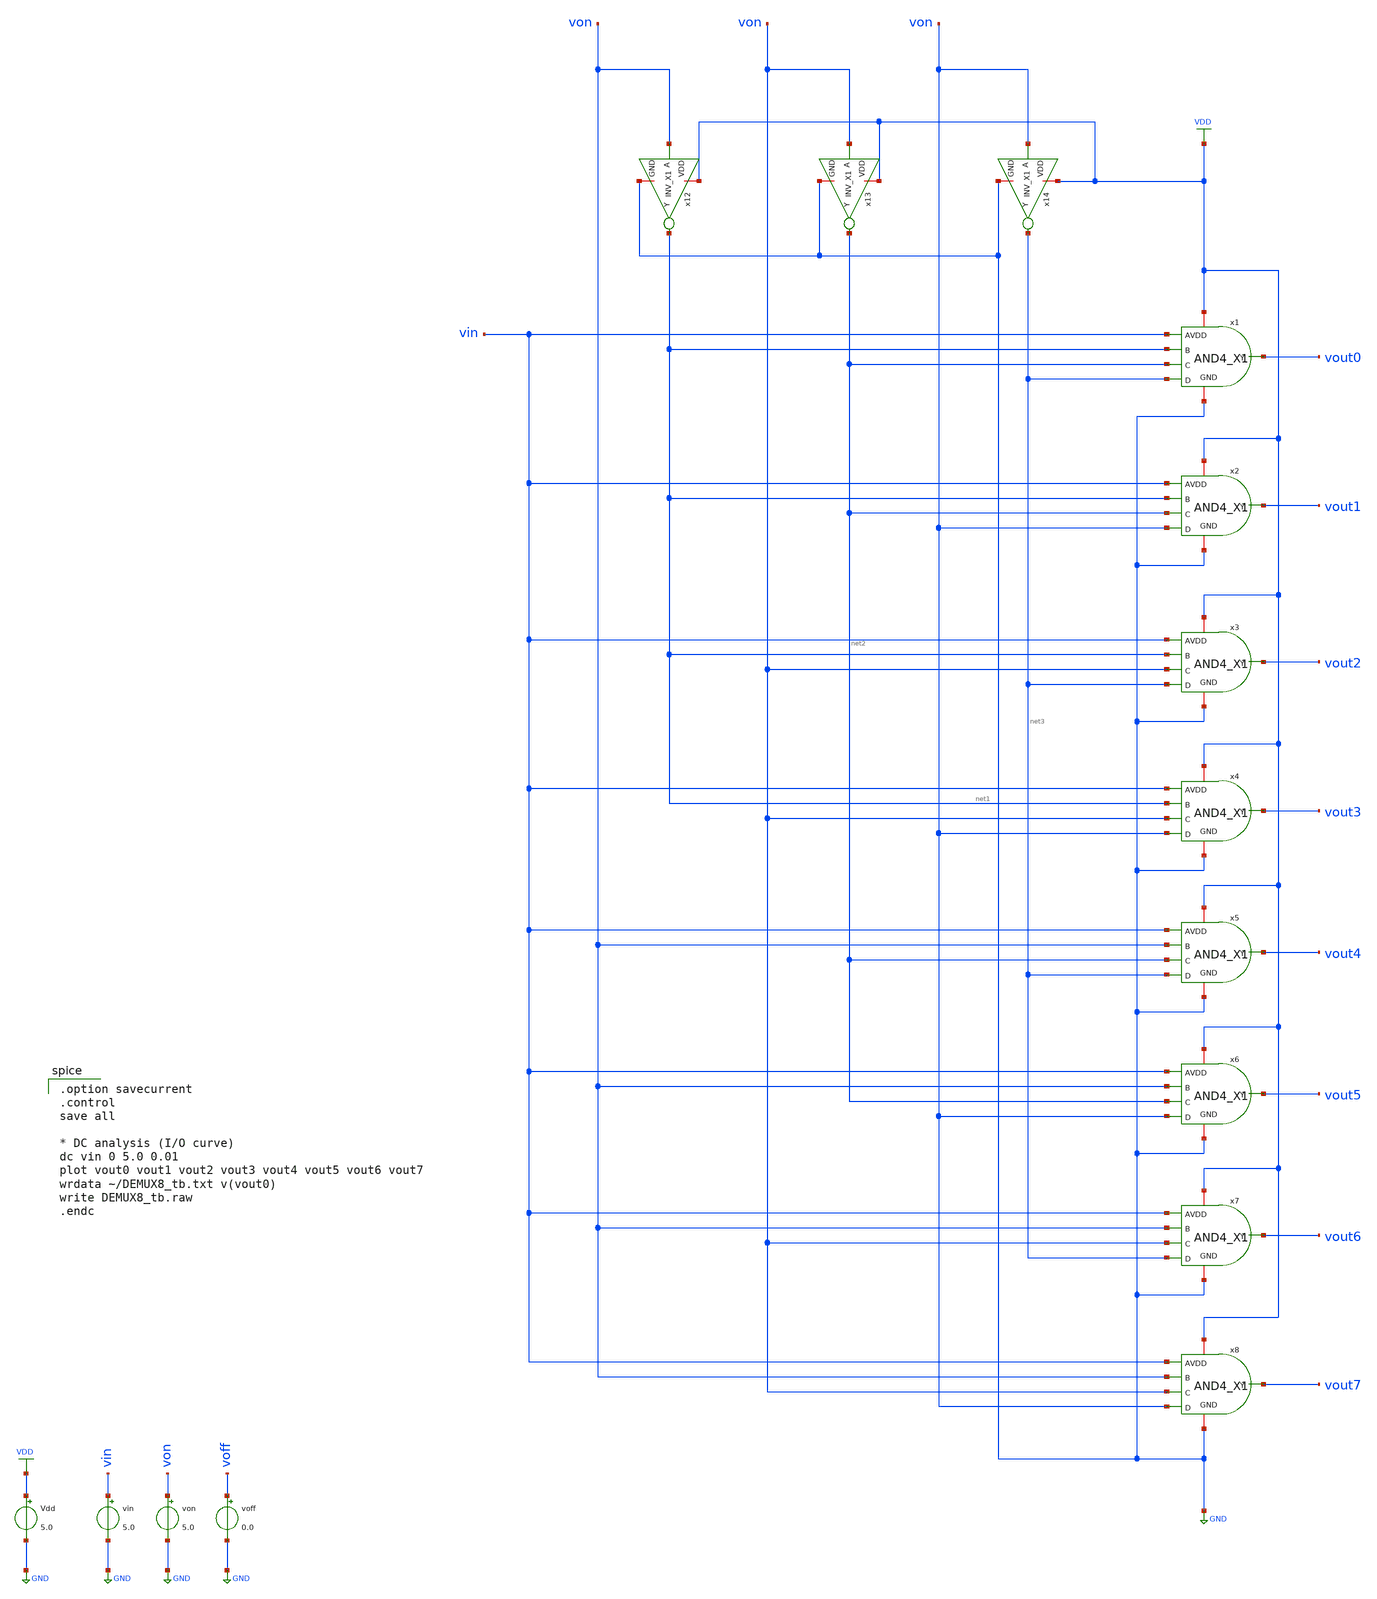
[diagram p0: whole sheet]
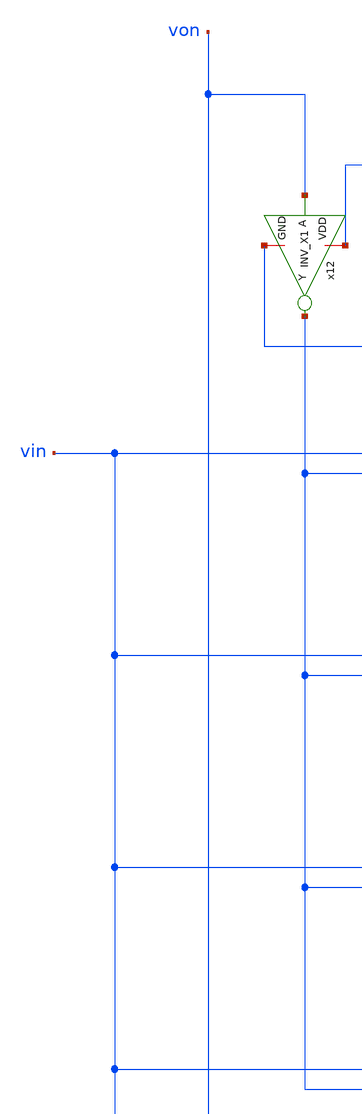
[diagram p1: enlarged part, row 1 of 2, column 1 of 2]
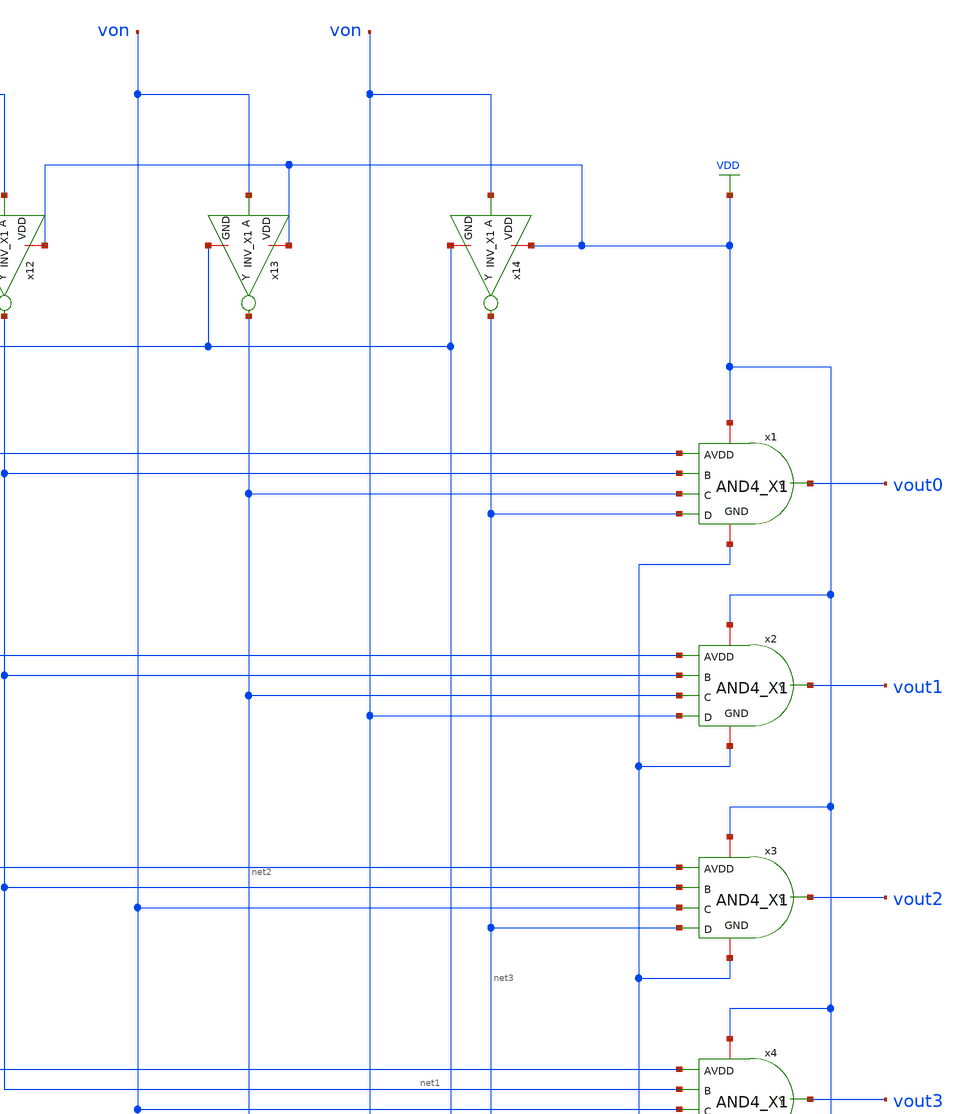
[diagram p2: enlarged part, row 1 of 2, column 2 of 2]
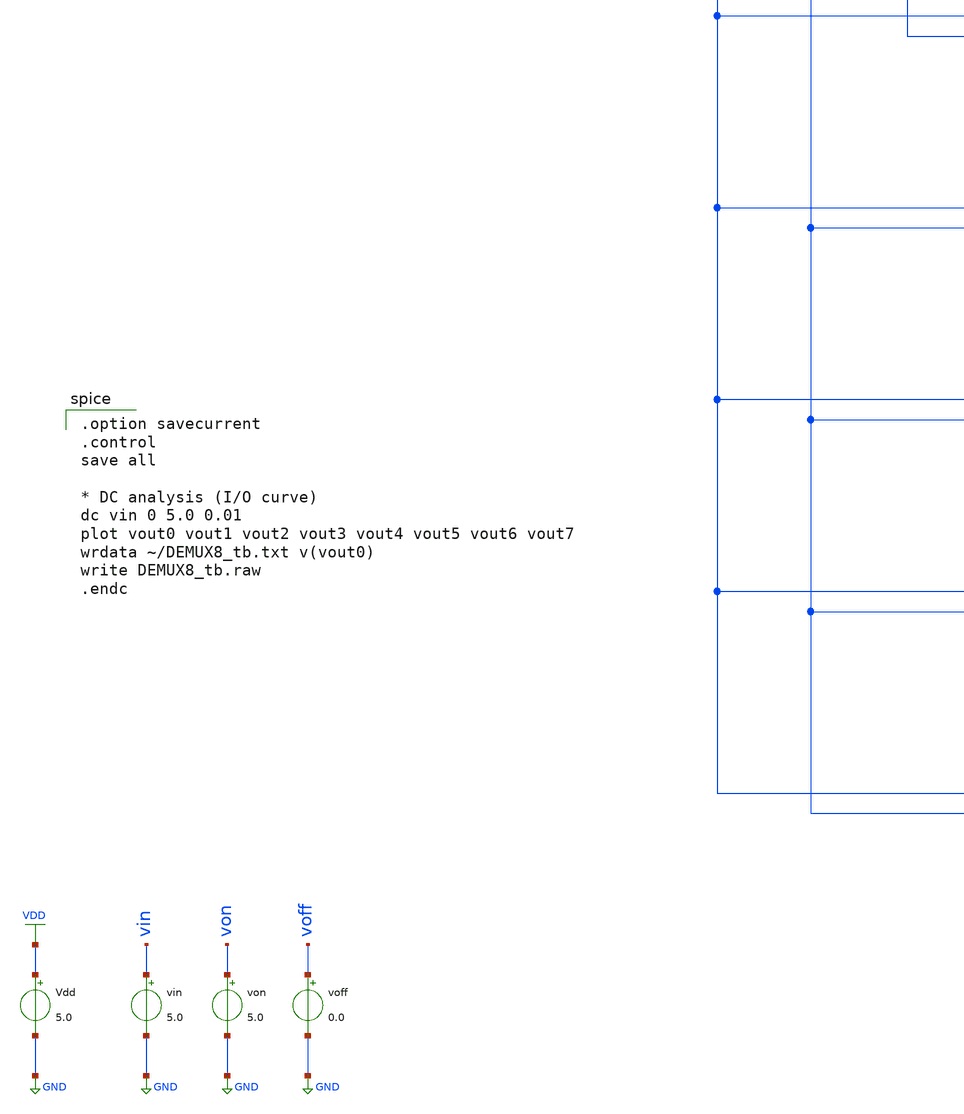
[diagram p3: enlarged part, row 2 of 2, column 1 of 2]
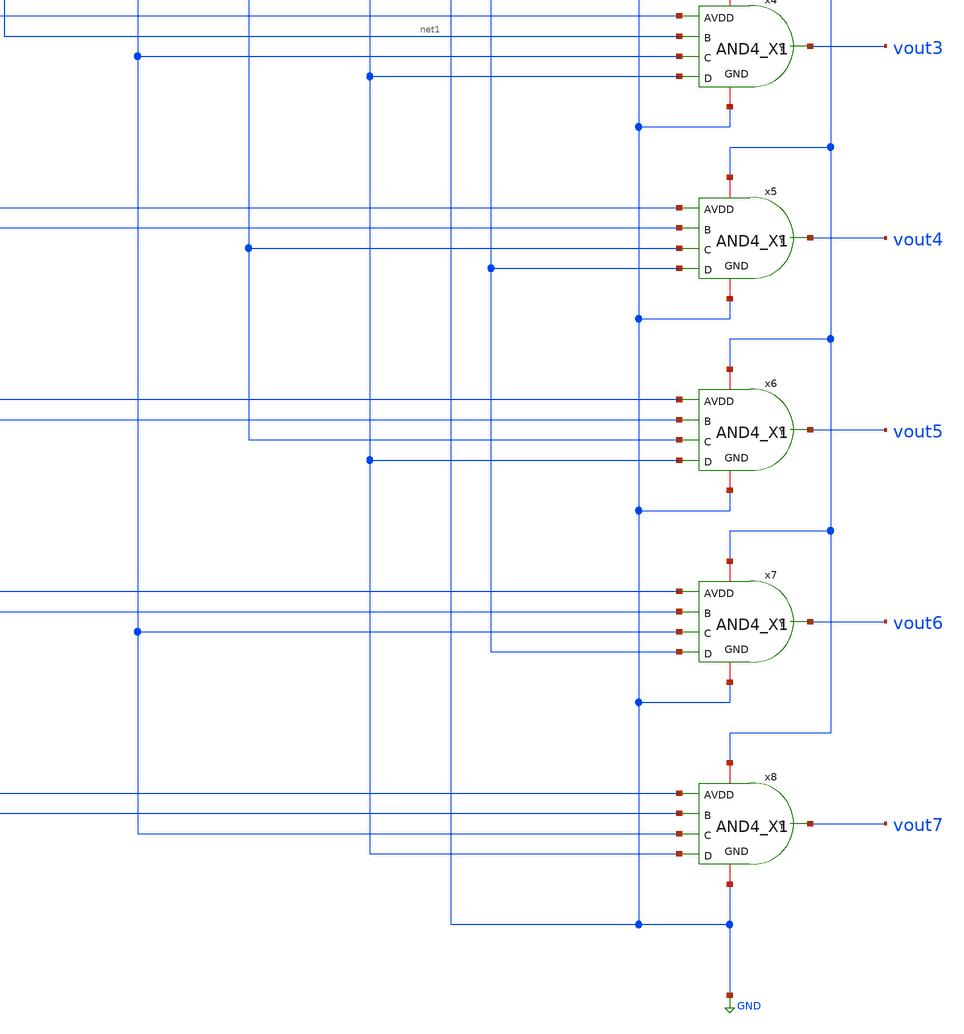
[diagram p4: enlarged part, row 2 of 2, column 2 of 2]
** sch_path: schematic/20250924_OSS_Workshop/Qdai/inverter_MUX_02/DEMUX8_tb.sch
**.subckt DEMUX8_tb
x1 net3 net2 VDD vout0 vin net1 GND AND4_X1
x2 von net2 VDD vout1 vin net1 GND AND4_X1
x3 net3 von VDD vout2 vin net1 GND AND4_X1
x4 von von VDD vout3 vin net1 GND AND4_X1
x5 net3 net2 VDD vout4 vin von GND AND4_X1
x6 von net2 VDD vout5 vin von GND AND4_X1
x7 net3 von VDD vout6 vin von GND AND4_X1
x8 von von VDD vout7 vin von GND AND4_X1
x12 VDD von net1 GND INV_X1
x13 VDD von net2 GND INV_X1
x14 VDD von net3 GND INV_X1
Vdd VDD GND 5.0
von von GND 5.0
voff voff GND 0.0
vin vin GND 5.0
**** begin user architecture code
 .include $::LIB/../ip62_models

.option savecurrent
.control
save all

* DC analysis (I/O curve)
dc vin 0 5.0 0.01
plot vout0 vout1 vout2 vout3 vout4 vout5 vout6 vout7
wrdata ~/DEMUX8_tb.txt v(vout0)
write DEMUX8_tb.raw
.endc

**** end user architecture code
**.ends

* expanding   symbol:  IP62_5_stdcell/AND4_X1.sym # of pins=7
** sym_path: openIP62_rev1.0/IP62/Technology/tech/symbols/Xschem/IP62_5_stdcell/AND4_X1.sym
** sch_path: openIP62_rev1.0/IP62/Technology/tech/symbols/Xschem/IP62_5_stdcell/AND4_X1.sch
.subckt AND4_X1 D C VDD Y A B GND
*.opin Y
*.ipin A
*.ipin B
*.iopin VDD
*.iopin GND
*.ipin C
*.ipin D
XM7 net1 A net4 GND NMOS w=3.4u l=1u as=0 ad=0 ps=0 pd=0 nrd=0 nrs=0 m=1
XM5 net3 C net2 GND NMOS w=3.4u l=1u as=0 ad=0 ps=0 pd=0 nrd=0 nrs=0 m=1
XM8 Y net1 GND GND NMOS w=3.4u l=1u as=0 ad=0 ps=0 pd=0 nrd=0 nrs=0 m=1
XM10 net2 D GND GND NMOS w=3.4u l=1u as=0 ad=0 ps=0 pd=0 nrd=0 nrs=0 m=1
XM6 net4 B net3 GND NMOS w=3.4u l=1u as=0 ad=0 ps=0 pd=0 nrd=0 nrs=0 m=1
XM11 net1 A VDD VDD PMOS w=10.2u l=1u as=0 ad=0 ps=0 pd=0 nrd=0 nrs=0 m=1
XM1 net1 D VDD VDD PMOS w=10.2u l=1u as=0 ad=0 ps=0 pd=0 nrd=0 nrs=0 m=1
XM3 net1 C VDD VDD PMOS w=10.2u l=1u as=0 ad=0 ps=0 pd=0 nrd=0 nrs=0 m=1
XM4 Y net1 VDD VDD PMOS w=10.2u l=1u as=0 ad=0 ps=0 pd=0 nrd=0 nrs=0 m=1
XM2 net1 B VDD VDD PMOS w=10.2u l=1u as=0 ad=0 ps=0 pd=0 nrd=0 nrs=0 m=1
.ends


* expanding   symbol:  IP62_5_stdcell/INV_X1.sym # of pins=4
** sym_path: openIP62_rev1.0/IP62/Technology/tech/symbols/Xschem/IP62_5_stdcell/INV_X1.sym
** sch_path: openIP62_rev1.0/IP62/Technology/tech/symbols/Xschem/IP62_5_stdcell/INV_X1.sch
.subckt INV_X1 VDD A Y GND
*.ipin A
*.opin Y
*.iopin GND
*.iopin VDD
XM7 Y A VDD VDD PMOS w=10.2u l=1u as=0 ad=0 ps=0 pd=0 nrd=0 nrs=0 m=1
XM2 Y A GND GND NMOS w=3.4u l=1u as=0 ad=0 ps=0 pd=0 nrd=0 nrs=0 m=1
.ends

.GLOBAL VDD
.GLOBAL GND
.end
